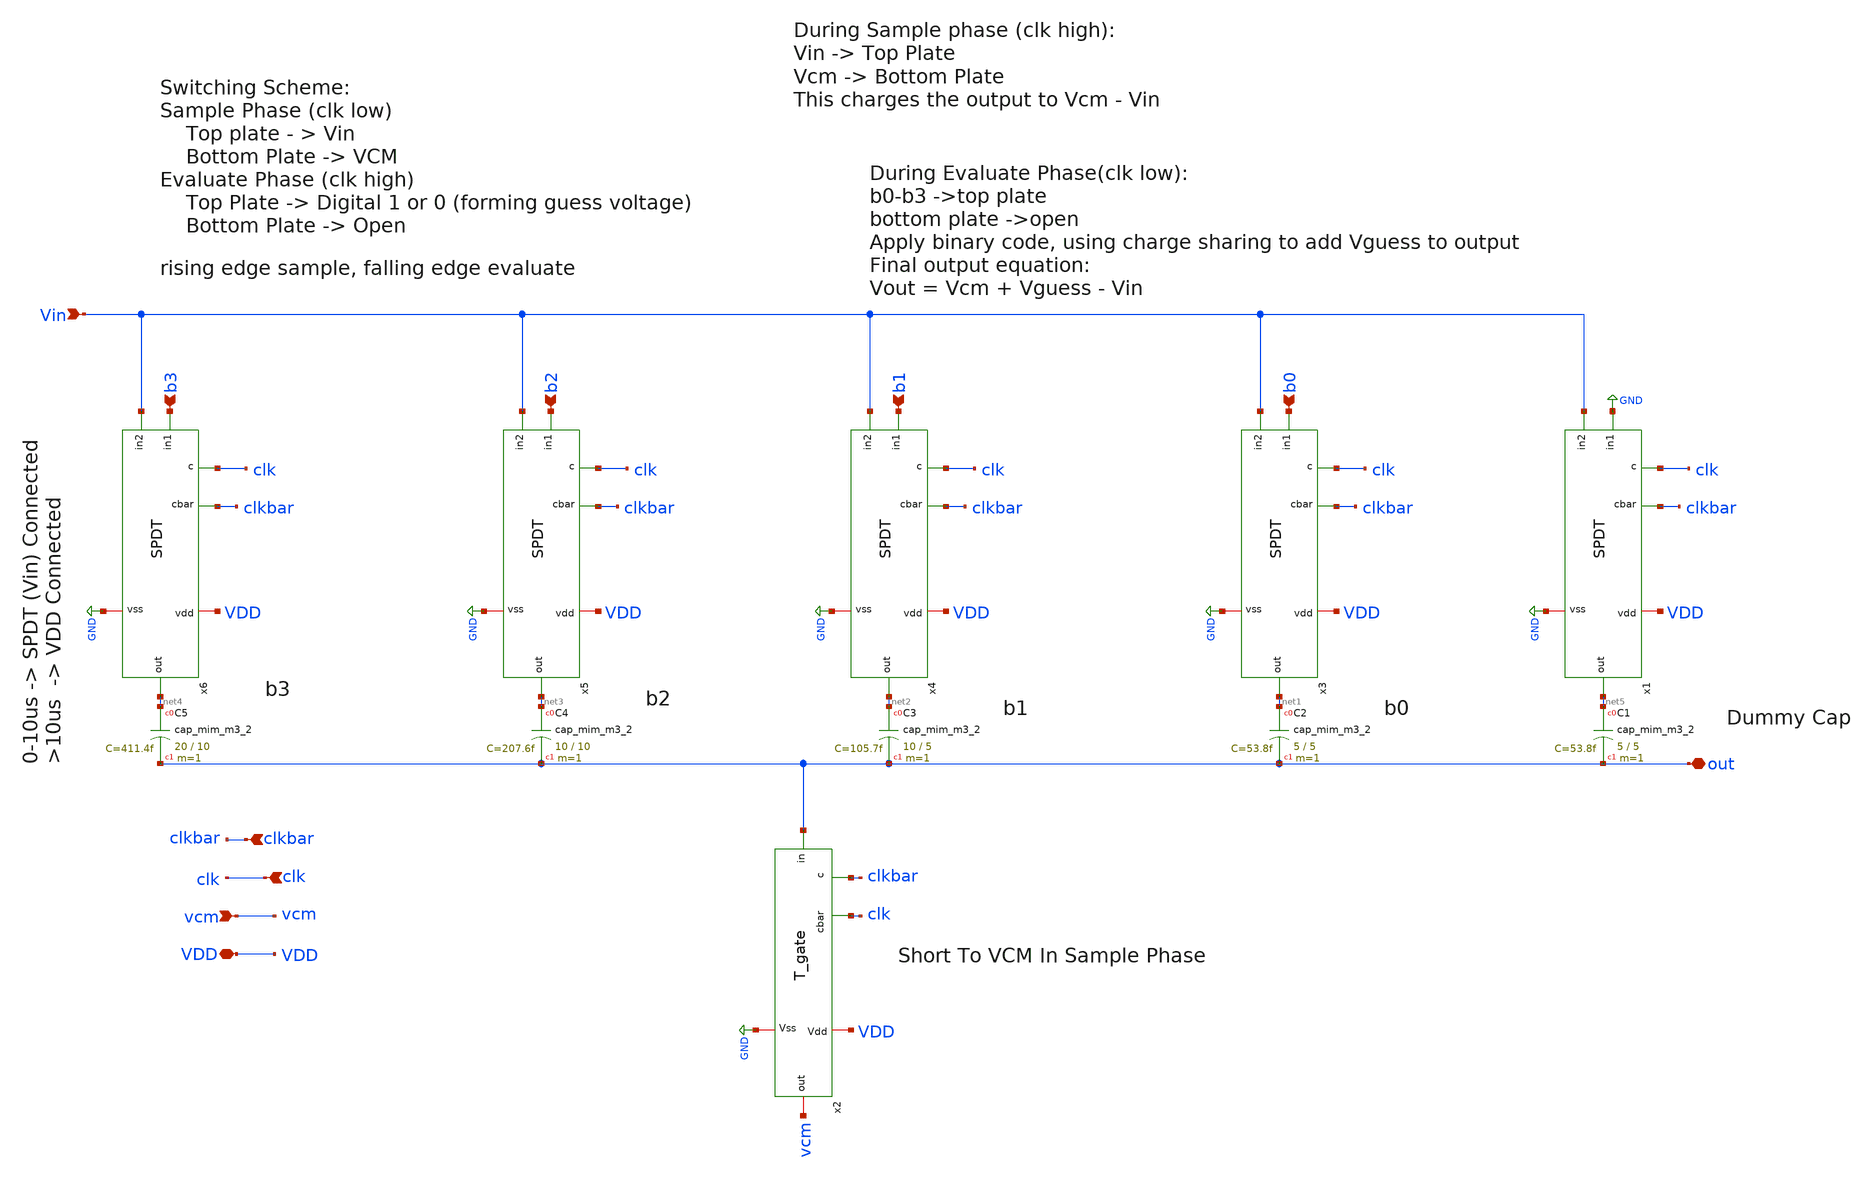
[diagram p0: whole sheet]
** sch_path: ADC/16bit_C2C/MagicAndSpice/CDAC_4bit_VCM_simplified.sch
**.subckt CDAC_4bit_VCM_simplified Vin clk clkbar vcm VDD b3 b2 b1 out b0
*.ipin Vin
*.ipin clk
*.ipin clkbar
*.ipin vcm
*.iopin VDD
*.ipin b3
*.ipin b2
*.ipin b1
*.iopin out
*.ipin b0
XC1 net5 out sky130_fd_pr__cap_mim_m3_2 W=5 L=5 MF=1 m=1
XC2 net1 out sky130_fd_pr__cap_mim_m3_2 W=5 L=5 MF=1 m=1
x2 clkbar vcm out VDD clk GND T_gate
x3 clkbar VDD GND clk b0 net1 Vin SPDT
XC3 net2 out sky130_fd_pr__cap_mim_m3_2 W=10 L=5 MF=1 m=1
x4 clkbar VDD GND clk b1 net2 Vin SPDT
XC4 net3 out sky130_fd_pr__cap_mim_m3_2 W=10 L=10 MF=1 m=1
x5 clkbar VDD GND clk b2 net3 Vin SPDT
XC5 net4 out sky130_fd_pr__cap_mim_m3_2 W=20 L=10 MF=1 m=1
x6 clkbar VDD GND clk b3 net4 Vin SPDT
x1 clkbar VDD GND clk GND net5 Vin SPDT
**.ends

* expanding   symbol:  /home/ee431/workspace/6SAR_CDAC/T_gate.sym # of pins=6
** sym_path: ADC/16bit_C2C/MagicAndSpice/T_gate.sym
** sch_path: ADC/16bit_C2C/MagicAndSpice/T_gate.sch
.subckt T_gate c out in Vdd cbar Vss
*.ipin in
*.ipin cbar
*.ipin c
*.iopin Vdd
*.iopin Vss
*.iopin out
XM1 in c out GND sky130_fd_pr__nfet_g5v0d10v5 L=1 W=10 nf=1 ad='int((nf+1)/2) * W/nf * 0.29' as='int((nf+2)/2) * W/nf * 0.29'
+ pd='2*int((nf+1)/2) * (W/nf + 0.29)' ps='2*int((nf+2)/2) * (W/nf + 0.29)' nrd='0.29 / W' nrs='0.29 / W'
+ sa=0 sb=0 sd=0 mult=1 m=1
XM2 out cbar in Vdd sky130_fd_pr__pfet_g5v0d10v5 L=1 W=10 nf=1 ad='int((nf+1)/2) * W/nf * 0.29' as='int((nf+2)/2) * W/nf * 0.29'
+ pd='2*int((nf+1)/2) * (W/nf + 0.29)' ps='2*int((nf+2)/2) * (W/nf + 0.29)' nrd='0.29 / W' nrs='0.29 / W'
+ sa=0 sb=0 sd=0 mult=1 m=1
.ends


* expanding   symbol:  /home/ee431/workspace/6SAR_CDAC/SPDT.sym # of pins=7
** sym_path: ADC/4bit_C2C/MagicAndSpice/SPDT.sym
** sch_path: ADC/4bit_C2C/MagicAndSpice/SPDT.sch
.subckt SPDT cbar vdd vss c in1 out in2
*.ipin in1
*.ipin in2
*.ipin c
*.ipin cbar
*.opin out
*.iopin vdd
*.iopin vss
x1 c out in1 vdd cbar vss T_gate
x2 cbar out in2 vdd c vss T_gate
.ends

.GLOBAL GND
.end
